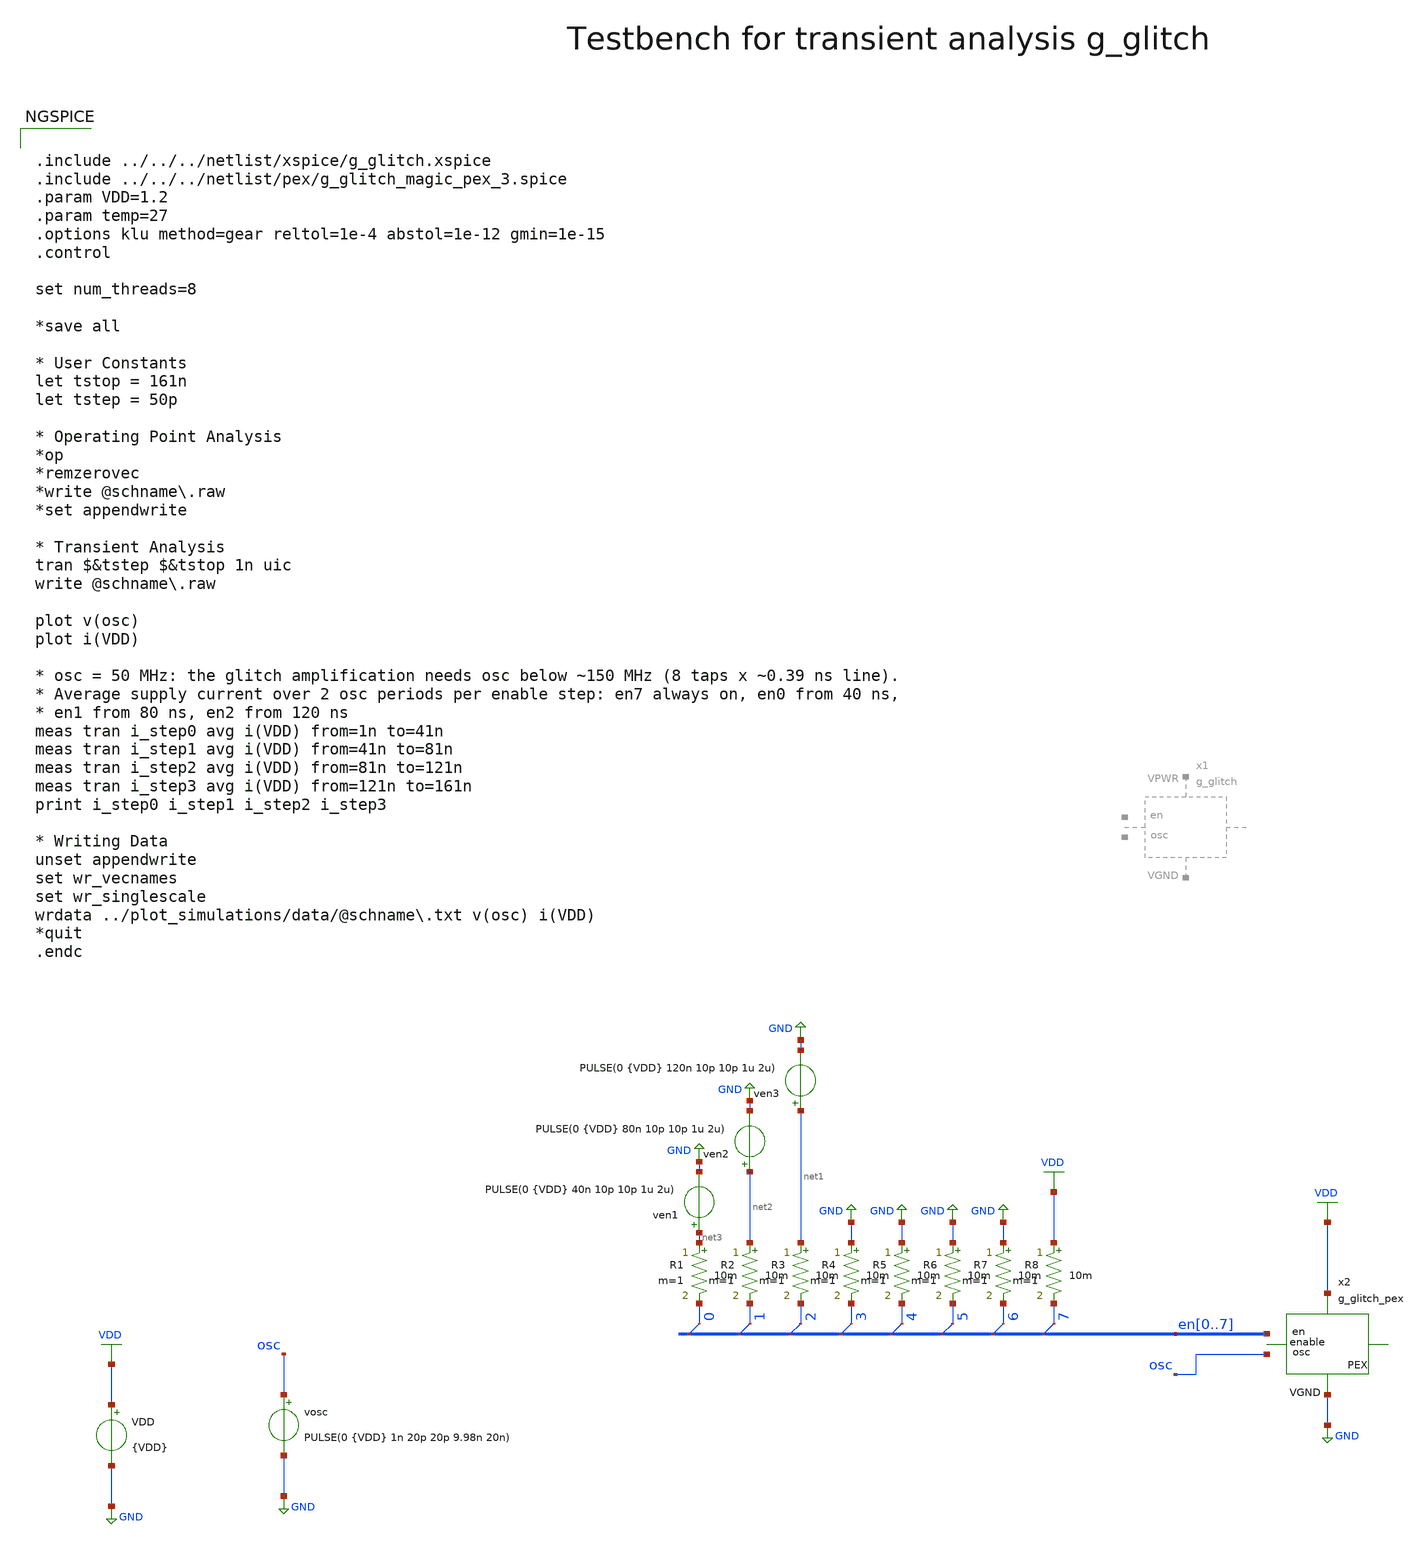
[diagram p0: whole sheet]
** sch_path: macros/heichips26_digital_project/macros/g_glitch/testbenches/xschem/g_glitch_tb_tran.sch
**.subckt g_glitch_tb_tran
VDD VDD GND {VDD}
ven1 net3 GND PULSE(0 {VDD} 40n 10p 10p 1u 2u)
x2 VDD GND osc en0 en1 en2 en3 en4 en5 en6 en7 g_glitch_pex
* tap: en[0..7] --> en0
* tap: en[0..7] --> en2
* tap: en[0..7] --> en4
* tap: en[0..7] --> en6
* tap: en[0..7] --> en7
* tap: en[0..7] --> en5
* tap: en[0..7] --> en3
* tap: en[0..7] --> en1
R1 net3 en0 10m m=1
R2 net2 en1 10m m=1
R3 net1 en2 10m m=1
R4 GND en3 10m m=1
R5 GND en4 10m m=1
R6 GND en5 10m m=1
R7 GND en6 10m m=1
R8 VDD en7 10m m=1
ven2 net2 GND PULSE(0 {VDD} 80n 10p 10p 1u 2u)
ven3 net1 GND PULSE(0 {VDD} 120n 10p 10p 1u 2u)
vosc osc GND PULSE(0 {VDD} 1n 20p 20p 9.98n 20n)
**** begin user architecture code


.include ../../../netlist/xspice/g_glitch.xspice
.include ../../../netlist/pex/g_glitch_magic_pex_3.spice
.param VDD=1.2
.param temp=27
.options klu method=gear reltol=1e-4 abstol=1e-12 gmin=1e-15
.control

set num_threads=8

*save all

* User Constants
let tstop = 161n
let tstep = 50p

* Operating Point Analysis
*op
*remzerovec
*write @schname\.raw
*set appendwrite

* Transient Analysis
tran $&tstep $&tstop 1n uic
write @schname\.raw

plot v(osc)
plot i(VDD)

* osc = 50 MHz: the glitch amplification needs osc below ~150 MHz (8 taps x ~0.39 ns line).
* Average supply current over 2 osc periods per enable step: en7 always on, en0 from 40 ns,
* en1 from 80 ns, en2 from 120 ns
meas tran i_step0 avg i(VDD) from=1n to=41n
meas tran i_step1 avg i(VDD) from=41n to=81n
meas tran i_step2 avg i(VDD) from=81n to=121n
meas tran i_step3 avg i(VDD) from=121n to=161n
print i_step0 i_step1 i_step2 i_step3

* Writing Data
unset appendwrite
set wr_vecnames
set wr_singlescale
wrdata ../plot_simulations/data/@schname\.txt v(osc) i(VDD)
*quit
.endc


.lib cornerMOSlv.lib mos_tt
.lib cornerMOShv.lib mos_tt
.lib cornerRES.lib res_typ
.lib cornerDIO.lib dio_tt

**** end user architecture code
**.ends
.GLOBAL GND
.GLOBAL VDD
.end
